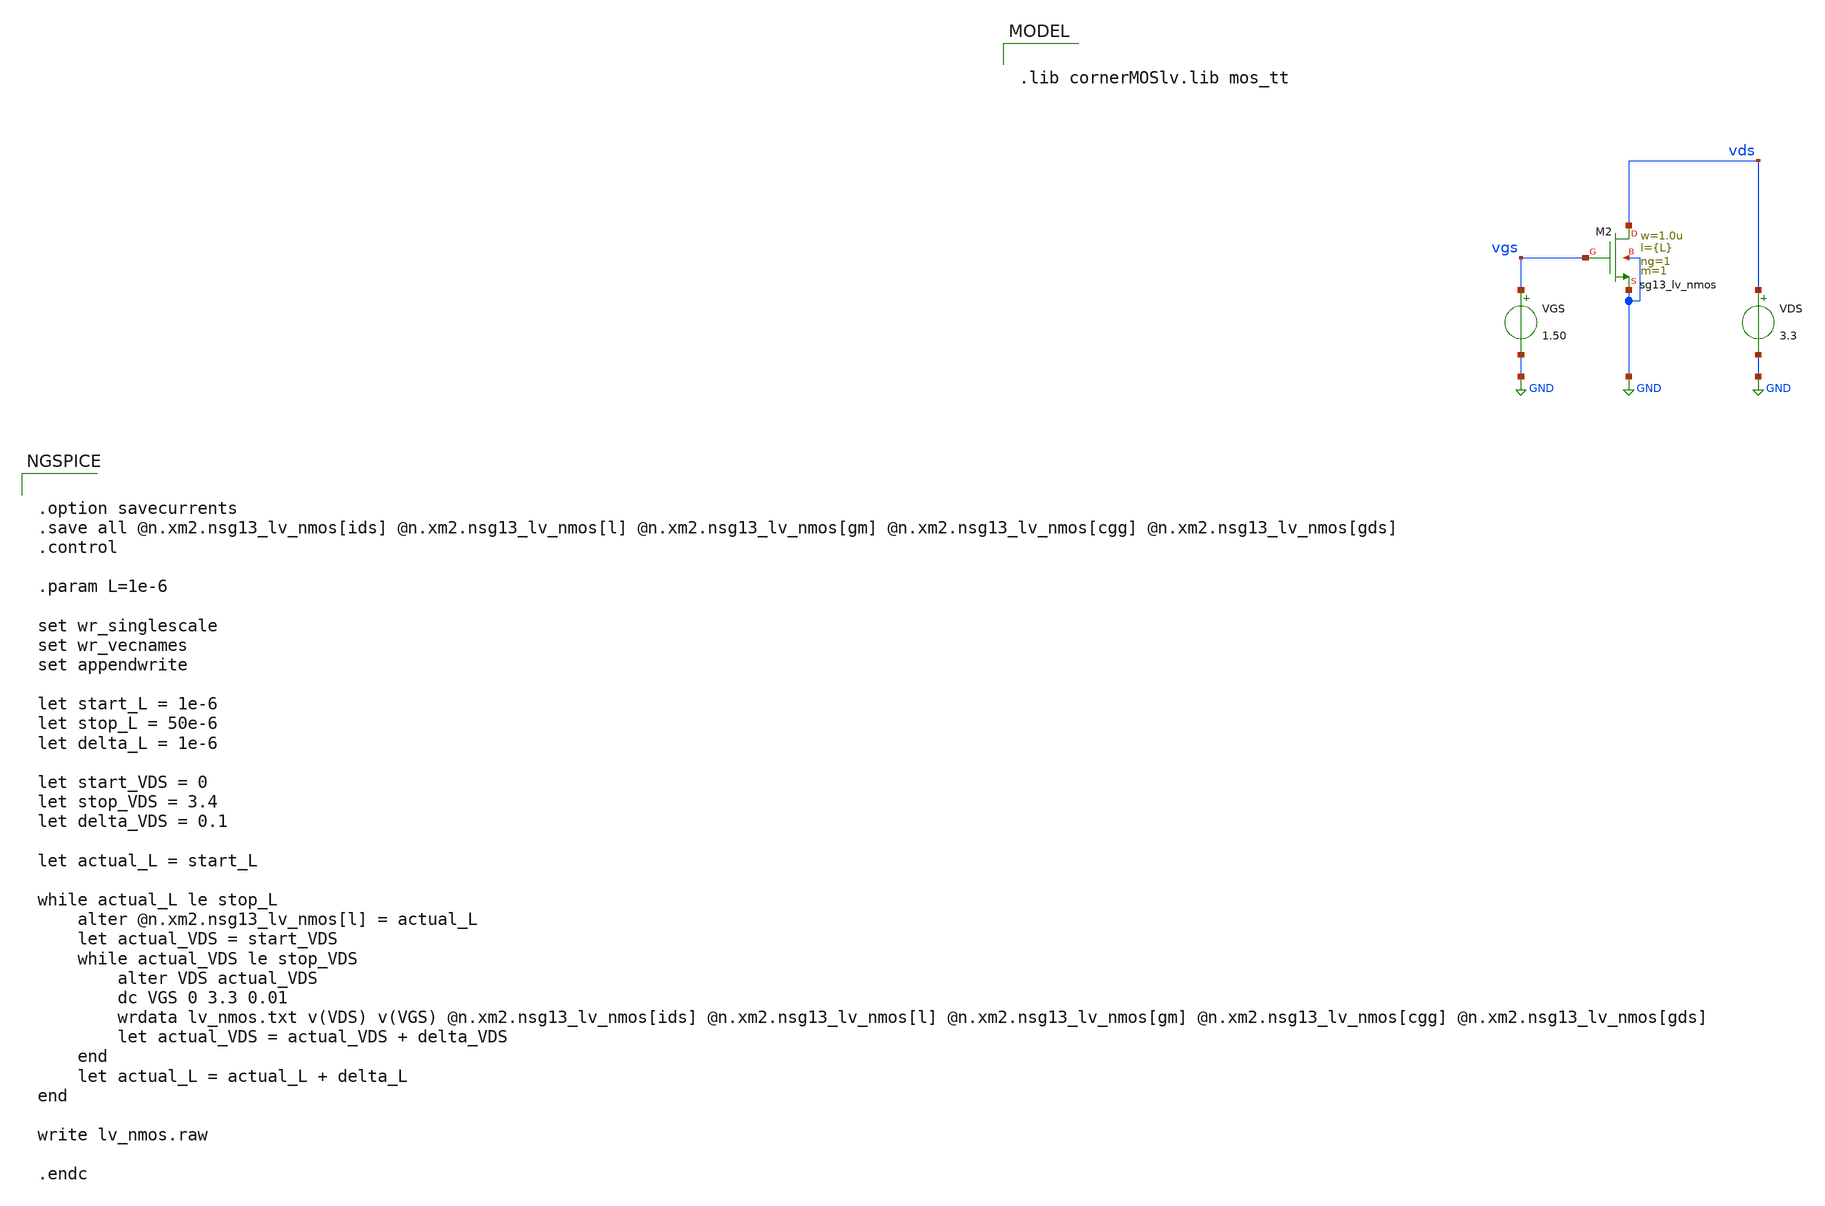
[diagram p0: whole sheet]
** sch_path: gmid/lv_nmos.sch
**.subckt lv_nmos
VGS vgs GND 1.50
VDS vds GND 3.3
XM2 vds vgs GND GND sg13_lv_nmos w=1.0u l={L} ng=1 m=1 mm_ok=1
**** begin user architecture code

.lib cornerMOSlv.lib mos_tt



.option savecurrents
.save all @n.xm2.nsg13_lv_nmos[ids] @n.xm2.nsg13_lv_nmos[l] @n.xm2.nsg13_lv_nmos[gm] @n.xm2.nsg13_lv_nmos[cgg] @n.xm2.nsg13_lv_nmos[gds]
.control

.param L=1e-6

set wr_singlescale
set wr_vecnames
set appendwrite

let start_L = 1e-6
let stop_L = 50e-6
let delta_L = 1e-6

let start_VDS = 0
let stop_VDS = 3.4
let delta_VDS = 0.1

let actual_L = start_L

while actual_L le stop_L
	alter @n.xm2.nsg13_lv_nmos[l] = actual_L
	let actual_VDS = start_VDS
	while actual_VDS le stop_VDS
		alter VDS actual_VDS
		dc VGS 0 3.3 0.01
		wrdata lv_nmos.txt v(VDS) v(VGS) @n.xm2.nsg13_lv_nmos[ids] @n.xm2.nsg13_lv_nmos[l]
+ @n.xm2.nsg13_lv_nmos[gm] @n.xm2.nsg13_lv_nmos[cgg] @n.xm2.nsg13_lv_nmos[gds]
		let actual_VDS = actual_VDS + delta_VDS
	end
	let actual_L = actual_L + delta_L
end

write lv_nmos.raw

.endc



**** end user architecture code
**.ends
.GLOBAL GND
.end
